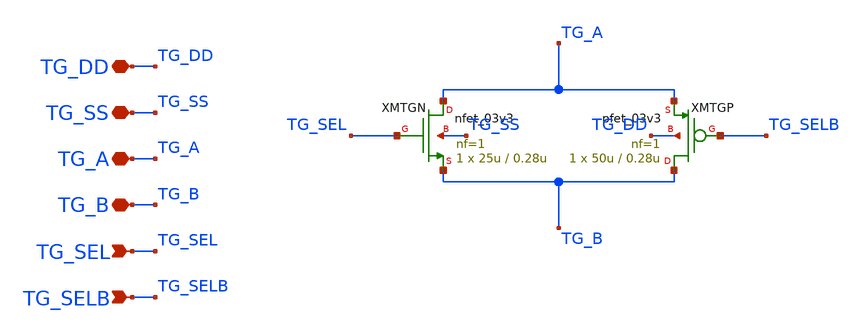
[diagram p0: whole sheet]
** sch_path: Design_Files/IC Design/Schematic/DIGITAL_BLOCKS/TG/TG.sch
**.subckt TG TG_DD TG_SS TG_A TG_B TG_SEL TG_SELB
*.iopin TG_DD
*.iopin TG_SS
*.iopin TG_A
*.iopin TG_B
*.ipin TG_SEL
*.ipin TG_SELB
XMTGP TG_B TG_SELB TG_A TG_DD pfet_03v3 L=0.28u W=50u nf=1 ad='int((nf+1)/2) * W/nf * 0.18u' as='int((nf+2)/2) * W/nf * 0.18u'
+ pd='2*int((nf+1)/2) * (W/nf + 0.18u)' ps='2*int((nf+2)/2) * (W/nf + 0.18u)' nrd='0.18u / W' nrs='0.18u / W'
+ sa=0 sb=0 sd=0 m=1
XMTGN TG_A TG_SEL TG_B TG_SS nfet_03v3 L=0.28u W=25u nf=1 ad='int((nf+1)/2) * W/nf * 0.18u' as='int((nf+2)/2) * W/nf * 0.18u'
+ pd='2*int((nf+1)/2) * (W/nf + 0.18u)' ps='2*int((nf+2)/2) * (W/nf + 0.18u)' nrd='0.18u / W' nrs='0.18u / W'
+ sa=0 sb=0 sd=0 m=1
**.ends
.end
